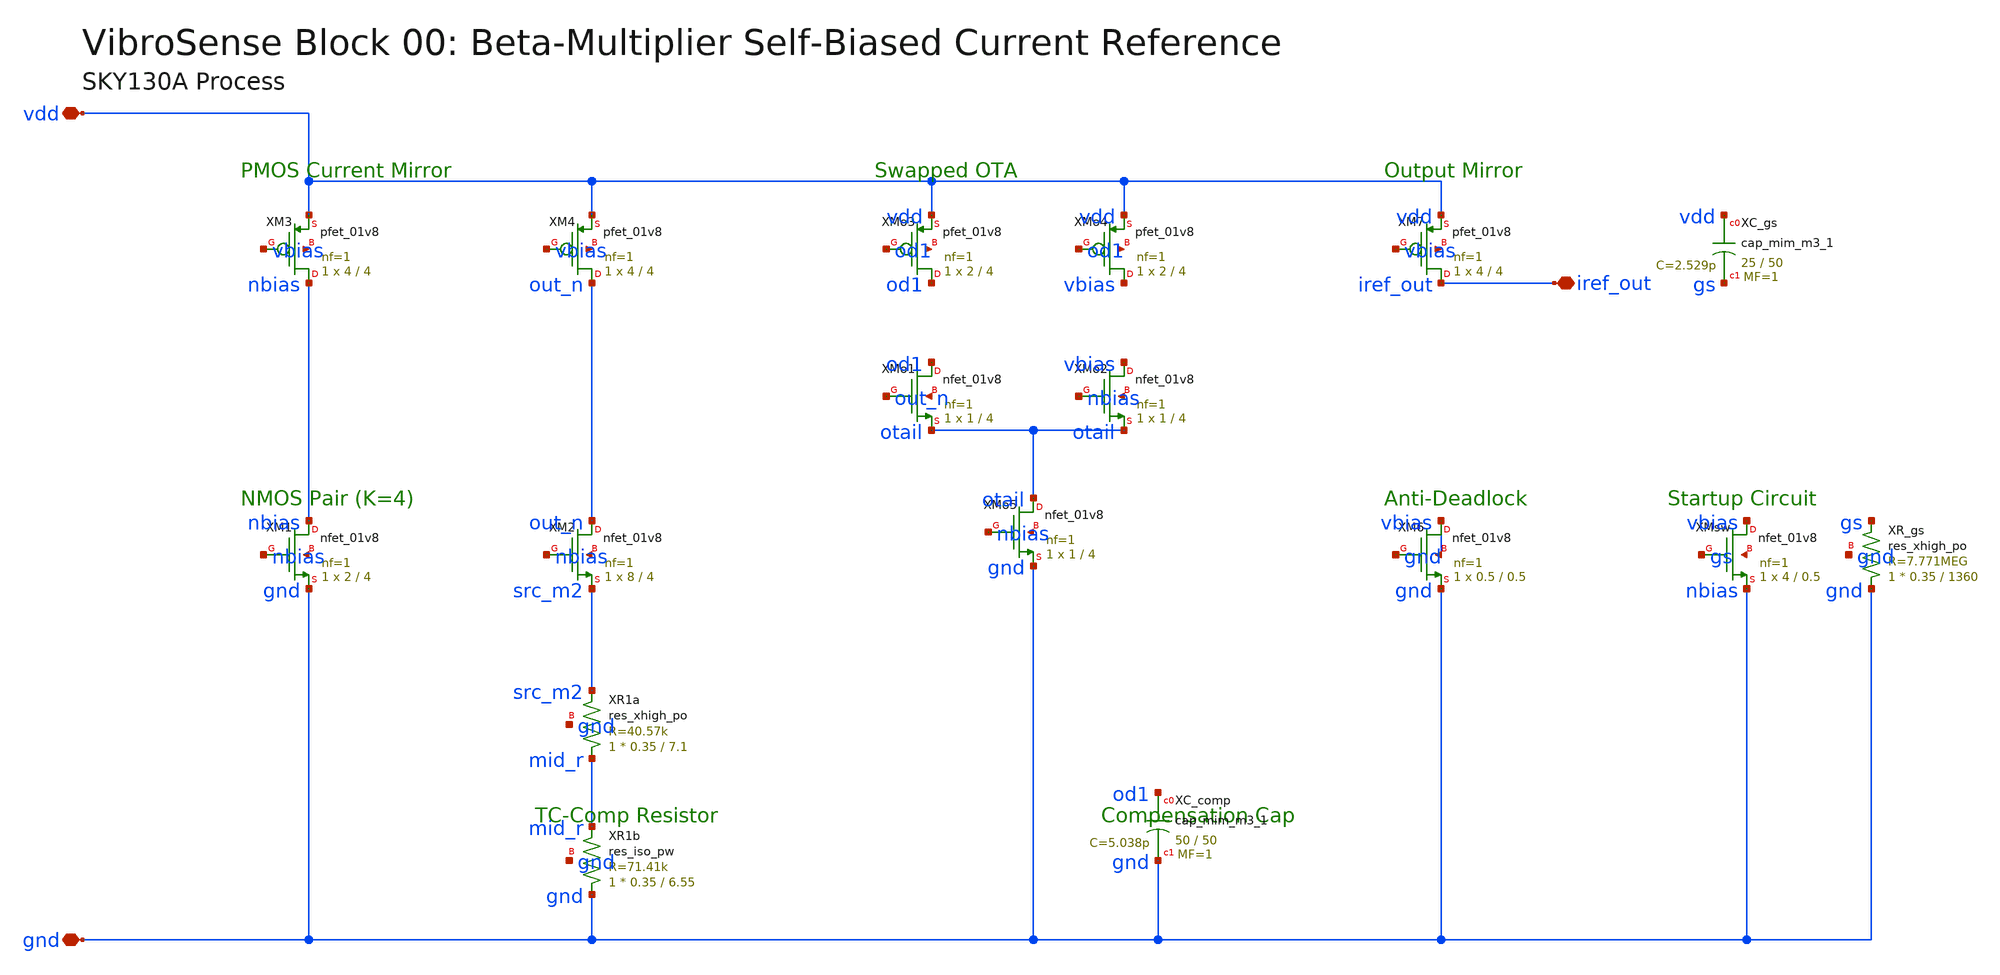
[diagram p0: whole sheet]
** sch_path: vibrosense/00_bias/bias_generator.sch
**.subckt bias_generator vdd gnd iref_out
*.iopin vdd
*.iopin gnd
*.iopin iref_out
XXM3 nbias vbias vdd net1 sky130_fd_pr__pfet_01v8 L=4 W=4 nf=1 ad='int((nf+1)/2) * W/nf * 0.29' as='int((nf+2)/2) * W/nf * 0.29'
+ pd='2*int((nf+1)/2) * (W/nf + 0.29)' ps='2*int((nf+2)/2) * (W/nf + 0.29)' nrd='0.29 / W' nrs='0.29 / W'
+ sa=0 sb=0 sd=0 mult=1 m=1
XXM4 out_n vbias vdd net2 sky130_fd_pr__pfet_01v8 L=4 W=4 nf=1 ad='int((nf+1)/2) * W/nf * 0.29' as='int((nf+2)/2) * W/nf * 0.29'
+ pd='2*int((nf+1)/2) * (W/nf + 0.29)' ps='2*int((nf+2)/2) * (W/nf + 0.29)' nrd='0.29 / W' nrs='0.29 / W'
+ sa=0 sb=0 sd=0 mult=1 m=1
XXM1 nbias nbias gnd net3 sky130_fd_pr__nfet_01v8 L=4 W=2 nf=1 ad='int((1 + 1)/2) * 2 / 1 * 0.29' as='int((1 + 2)/2) * 2 / 1 * 0.29'
+ pd='2*int((1 + 1)/2) * (2 / 1 + 0.29)' ps='2*int((1 + 2)/2) * (2 / 1 + 0.29)' nrd='0.29 / 2 ' nrs='0.29 / 2 '
+ sa=0 sb=0 sd=0 mult=1 m=1
XXM2 out_n nbias src_m2 net4 sky130_fd_pr__nfet_01v8 L=4 W=8 nf=1 ad='int((1 + 1)/2) * 8 / 1 * 0.29'
+ as='int((1 + 2)/2) * 8 / 1 * 0.29' pd='2*int((1 + 1)/2) * (8 / 1 + 0.29)' ps='2*int((1 + 2)/2) * (8 / 1 + 0.29)'
+ nrd='0.29 / 8 ' nrs='0.29 / 8 ' sa=0 sb=0 sd=0 mult=1 m=1
XXR1a mid_r src_m2 gnd sky130_fd_pr__res_xhigh_po W=0.35 L=7.1 mult=1 m=1
XXR1b gnd mid_r gnd sky130_fd_pr__res_iso_pw W=0.35 L=6.55 m=1
XXMo1 od1 out_n otail net5 sky130_fd_pr__nfet_01v8 L=4 W=1 nf=1 ad='int((1 + 1)/2) * 1 / 1 * 0.29' as='int((1 + 2)/2) * 1 / 1 * 0.29'
+ pd='2*int((1 + 1)/2) * (1 / 1 + 0.29)' ps='2*int((1 + 2)/2) * (1 / 1 + 0.29)' nrd='0.29 / 1 ' nrs='0.29 / 1 '
+ sa=0 sb=0 sd=0 mult=1 m=1
XXMo2 vbias nbias otail net6 sky130_fd_pr__nfet_01v8 L=4 W=1 nf=1 ad='int((1 + 1)/2) * 1 / 1 * 0.29'
+ as='int((1 + 2)/2) * 1 / 1 * 0.29' pd='2*int((1 + 1)/2) * (1 / 1 + 0.29)' ps='2*int((1 + 2)/2) * (1 / 1 + 0.29)'
+ nrd='0.29 / 1 ' nrs='0.29 / 1 ' sa=0 sb=0 sd=0 mult=1 m=1
XXMo3 od1 od1 vdd net7 sky130_fd_pr__pfet_01v8 L=4 W=2 nf=1 ad='int((nf+1)/2) * W/nf * 0.29' as='int((nf+2)/2) * W/nf * 0.29'
+ pd='2*int((nf+1)/2) * (W/nf + 0.29)' ps='2*int((nf+2)/2) * (W/nf + 0.29)' nrd='0.29 / W' nrs='0.29 / W'
+ sa=0 sb=0 sd=0 mult=1 m=1
XXMo4 vbias od1 vdd net8 sky130_fd_pr__pfet_01v8 L=4 W=2 nf=1 ad='int((nf+1)/2) * W/nf * 0.29' as='int((nf+2)/2) * W/nf * 0.29'
+ pd='2*int((nf+1)/2) * (W/nf + 0.29)' ps='2*int((nf+2)/2) * (W/nf + 0.29)' nrd='0.29 / W' nrs='0.29 / W'
+ sa=0 sb=0 sd=0 mult=1 m=1
XXMo5 otail nbias gnd net9 sky130_fd_pr__nfet_01v8 L=4 W=1 nf=1 ad='int((1 + 1)/2) * 1 / 1 * 0.29' as='int((1 + 2)/2) * 1 / 1 * 0.29'
+ pd='2*int((1 + 1)/2) * (1 / 1 + 0.29)' ps='2*int((1 + 2)/2) * (1 / 1 + 0.29)' nrd='0.29 / 1 ' nrs='0.29 / 1 '
+ sa=0 sb=0 sd=0 mult=1 m=1
XXC_comp od1 gnd sky130_fd_pr__cap_mim_m3_1 W=50 L=50 MF=1 m=1
XXM7 iref_out vbias vdd net10 sky130_fd_pr__pfet_01v8 L=4 W=4 nf=1 ad='int((nf+1)/2) * W/nf * 0.29' as='int((nf+2)/2) * W/nf * 0.29'
+ pd='2*int((nf+1)/2) * (W/nf + 0.29)' ps='2*int((nf+2)/2) * (W/nf + 0.29)' nrd='0.29 / W' nrs='0.29 / W'
+ sa=0 sb=0 sd=0 mult=1 m=1
XXM6 vbias gnd gnd vbias sky130_fd_pr__nfet_01v8 L=0.5 W=0.5 nf=1 ad='int((1 + 1)/2) * 0.5 / 1 * 0.29'
+ as='int((1 + 2)/2) * 0.5 / 1 * 0.29' pd='2*int((1 + 1)/2) * (0.5 / 1 + 0.29)' ps='2*int((1 + 2)/2) * (0.5 / 1 + 0.29)'
+ nrd='0.29 / 0.5 ' nrs='0.29 / 0.5 ' sa=0 sb=0 sd=0 mult=1 m=1
XXC_gs vdd gs sky130_fd_pr__cap_mim_m3_1 W=25 L=50 MF=1 m=1
XXR_gs gnd gs gnd sky130_fd_pr__res_xhigh_po W=0.35 L=1360 mult=1 m=1
XXMsw vbias gs gnd net11 sky130_fd_pr__nfet_01v8 L=0.5 W=4 nf=1 ad='int((1 + 1)/2) * 4 / 1 * 0.29' as='int((1 + 2)/2) * 4 / 1 * 0.29'
+ pd='2*int((1 + 1)/2) * (4 / 1 + 0.29)' ps='2*int((1 + 2)/2) * (4 / 1 + 0.29)' nrd='0.29 / 4 ' nrs='0.29 / 4 '
+ sa=0 sb=0 sd=0 mult=1 m=1
**.ends
.end
